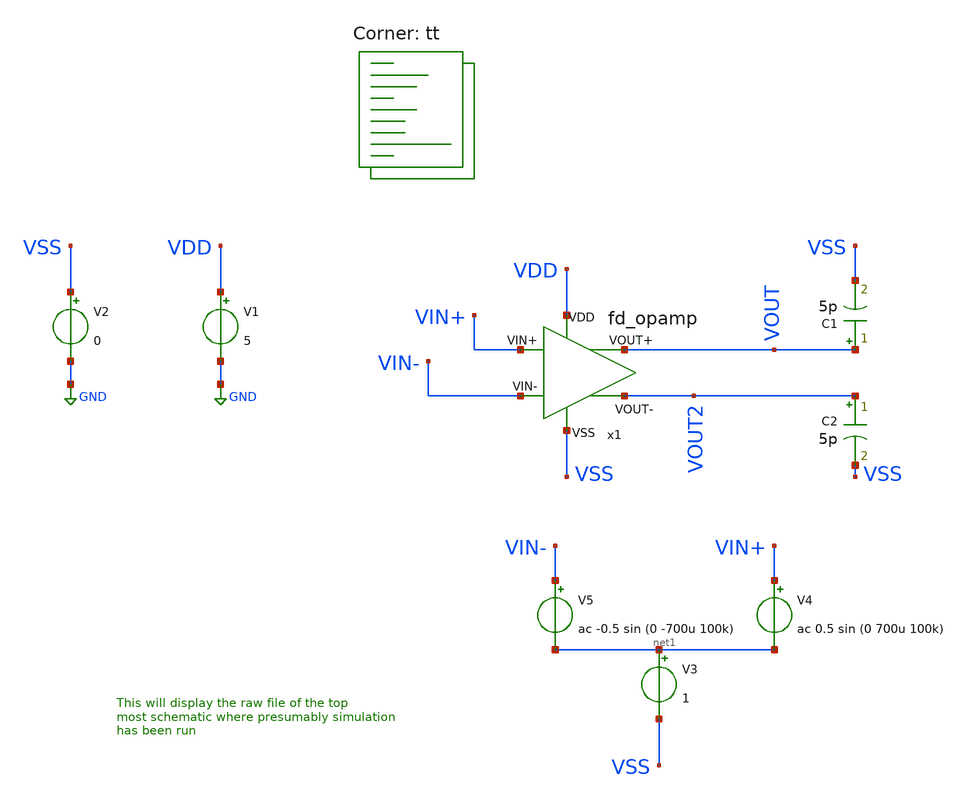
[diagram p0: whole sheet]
** sch_path: my_ip/sky130A/fully_differential_telescopic_cascode_5V_V1/tb/tb.sch
**.subckt tb
V1 VDD GND 5
V2 VSS GND 0
V3 net1 VSS 1
V4 VIN+ net1 ac 0.5 sin (0 700u 100k)
V5 VIN- net1 ac -0.5 sin (0 -700u 100k)
x1 VDD VSS VIN+ VOUT VIN- VOUT2 fd_opamp
C1 VOUT VSS 5p m=1
C2 VOUT2 VSS 5p m=1
**** begin user architecture code
.lib $::SKYWATER_MODELS/sky130.lib.spice tt
**** end user architecture code
**.ends
.GLOBAL GND
**** begin user architecture code


* ngspice commands
.options savecurrents
.TEMP 27
.control
save all
save @m.x1.xm1.msky130_fd_pr__pfet_g5v0d10v5[gm]
save @m.x1.xm1.msky130_fd_pr__pfet_g5v0d10v5[vth]
save @m.x1.xm1.msky130_fd_pr__pfet_g5v0d10v5[vds]
save @m.x1.xm1.msky130_fd_pr__pfet_g5v0d10v5[vgs]

save @m.x1.xm2.msky130_fd_pr__pfet_g5v0d10v5[gm]
save @m.x1.xm2.msky130_fd_pr__pfet_g5v0d10v5[vth]
save @m.x1.xm2.msky130_fd_pr__pfet_g5v0d10v5[vds]
save @m.x1.xm2.msky130_fd_pr__pfet_g5v0d10v5[vgs]

save @m.x1.xm3.msky130_fd_pr__pfet_g5v0d10v5[gm]
save @m.x1.xm3.msky130_fd_pr__pfet_g5v0d10v5[vth]
save @m.x1.xm3.msky130_fd_pr__pfet_g5v0d10v5[vds]
save @m.x1.xm3.msky130_fd_pr__pfet_g5v0d10v5[vgs]

save @m.x1.xm4.msky130_fd_pr__pfet_g5v0d10v5[gm]
save @m.x1.xm4.msky130_fd_pr__pfet_g5v0d10v5[vth]
save @m.x1.xm4.msky130_fd_pr__pfet_g5v0d10v5[vds]
save @m.x1.xm4.msky130_fd_pr__pfet_g5v0d10v5[vgs]

save @m.x1.xm5.msky130_fd_pr__nfet_g5v0d10v5[gm]
save @m.x1.xm5.msky130_fd_pr__nfet_g5v0d10v5[vth]
save @m.x1.xm5.msky130_fd_pr__nfet_g5v0d10v5[vds]
save @m.x1.xm5.msky130_fd_pr__nfet_g5v0d10v5[vgs]

save @m.x1.xm6.msky130_fd_pr__nfet_g5v0d10v5[gm]
save @m.x1.xm6.msky130_fd_pr__nfet_g5v0d10v5[vth]
save @m.x1.xm6.msky130_fd_pr__nfet_g5v0d10v5[vds]
save @m.x1.xm6.msky130_fd_pr__nfet_g5v0d10v5[vgs]

save @m.x1.xm7.msky130_fd_pr__nfet_g5v0d10v5[gm]
save @m.x1.xm7.msky130_fd_pr__nfet_g5v0d10v5[vth]
save @m.x1.xm7.msky130_fd_pr__nfet_g5v0d10v5[vds]
save @m.x1.xm7.msky130_fd_pr__nfet_g5v0d10v5[vgs]

save @m.x1.xm8.msky130_fd_pr__nfet_g5v0d10v5[gm]
save @m.x1.xm8.msky130_fd_pr__nfet_g5v0d10v5[vth]
save @m.x1.xm8.msky130_fd_pr__nfet_g5v0d10v5[vds]
save @m.x1.xm8.msky130_fd_pr__nfet_g5v0d10v5[vgs]

save @m.x1.xm9.msky130_fd_pr__pfet_g5v0d10v5[gm]
save @m.x1.xm9.msky130_fd_pr__pfet_g5v0d10v5[vth]
save @m.x1.xm9.msky130_fd_pr__pfet_g5v0d10v5[vds]
save @m.x1.xm9.msky130_fd_pr__pfet_g5v0d10v5[vgs]

save @m.x1.xm10.msky130_fd_pr__pfet_g5v0d10v5[gm]
save @m.x1.xm10.msky130_fd_pr__pfet_g5v0d10v5[vth]
save @m.x1.xm10.msky130_fd_pr__pfet_g5v0d10v5[vds]
save @m.x1.xm10.msky130_fd_pr__pfet_g5v0d10v5[vgs]

save @m.x1.xm11.msky130_fd_pr__pfet_g5v0d10v5[gm]
save @m.x1.xm11.msky130_fd_pr__pfet_g5v0d10v5[vth]
save @m.x1.xm11.msky130_fd_pr__pfet_g5v0d10v5[vds]
save @m.x1.xm11.msky130_fd_pr__pfet_g5v0d10v5[vgs]

save @m.x1.xm12.msky130_fd_pr__pfet_g5v0d10v5[gm]
save @m.x1.xm12.msky130_fd_pr__pfet_g5v0d10v5[vth]
save @m.x1.xm12.msky130_fd_pr__pfet_g5v0d10v5[vds]
save @m.x1.xm12.msky130_fd_pr__pfet_g5v0d10v5[vgs]

save @m.x1.xm13.msky130_fd_pr__nfet_g5v0d10v5[gm]
save @m.x1.xm13.msky130_fd_pr__nfet_g5v0d10v5[vth]
save @m.x1.xm13.msky130_fd_pr__nfet_g5v0d10v5[vds]
save @m.x1.xm13.msky130_fd_pr__nfet_g5v0d10v5[vgs]

save @m.x1.xm14.msky130_fd_pr__nfet_g5v0d10v5[gm]
save @m.x1.xm14.msky130_fd_pr__nfet_g5v0d10v5[vth]
save @m.x1.xm14.msky130_fd_pr__nfet_g5v0d10v5[vds]
save @m.x1.xm14.msky130_fd_pr__nfet_g5v0d10v5[vgs]

save @m.x1.xm15.msky130_fd_pr__nfet_g5v0d10v5[gm]
save @m.x1.xm15.msky130_fd_pr__nfet_g5v0d10v5[vth]
save @m.x1.xm15.msky130_fd_pr__nfet_g5v0d10v5[vds]
save @m.x1.xm15.msky130_fd_pr__nfet_g5v0d10v5[vgs]

save @m.x1.xm16.msky130_fd_pr__nfet_g5v0d10v5[gm]
save @m.x1.xm16.msky130_fd_pr__nfet_g5v0d10v5[vth]
save @m.x1.xm16.msky130_fd_pr__nfet_g5v0d10v5[vds]
save @m.x1.xm16.msky130_fd_pr__nfet_g5v0d10v5[vgs]


save @m.x1.xm17.msky130_fd_pr__pfet_g5v0d10v5[gm]
save @m.x1.xm17.msky130_fd_pr__pfet_g5v0d10v5[vth]
save @m.x1.xm17.msky130_fd_pr__pfet_g5v0d10v5[vds]
save @m.x1.xm17.msky130_fd_pr__pfet_g5v0d10v5[vgs]

save @m.x1.xm18.msky130_fd_pr__pfet_g5v0d10v5[gm]
save @m.x1.xm18.msky130_fd_pr__pfet_g5v0d10v5[vth]
save @m.x1.xm18.msky130_fd_pr__pfet_g5v0d10v5[vds]
save @m.x1.xm18.msky130_fd_pr__pfet_g5v0d10v5[vgs]

save @m.x1.xm19.msky130_fd_pr__pfet_g5v0d10v5[gm]
save @m.x1.xm19.msky130_fd_pr__pfet_g5v0d10v5[vth]
save @m.x1.xm19.msky130_fd_pr__pfet_g5v0d10v5[vds]
save @m.x1.xm19.msky130_fd_pr__pfet_g5v0d10v5[vgs]

save @m.x1.xm20.msky130_fd_pr__pfet_g5v0d10v5[gm]
save @m.x1.xm20.msky130_fd_pr__pfet_g5v0d10v5[vth]
save @m.x1.xm20.msky130_fd_pr__pfet_g5v0d10v5[vds]
save @m.x1.xm20.msky130_fd_pr__pfet_g5v0d10v5[vgs]

save @m.x1.xm21.msky130_fd_pr__pfet_g5v0d10v5[gm]
save @m.x1.xm21.msky130_fd_pr__pfet_g5v0d10v5[vth]
save @m.x1.xm21.msky130_fd_pr__pfet_g5v0d10v5[vds]
save @m.x1.xm21.msky130_fd_pr__pfet_g5v0d10v5[vgs]

save @m.x1.xm22.msky130_fd_pr__pfet_g5v0d10v5[gm]
save @m.x1.xm22.msky130_fd_pr__pfet_g5v0d10v5[vth]
save @m.x1.xm22.msky130_fd_pr__pfet_g5v0d10v5[vds]
save @m.x1.xm22.msky130_fd_pr__pfet_g5v0d10v5[vgs]

save @m.x1.xm23.msky130_fd_pr__nfet_g5v0d10v5[gm]
save @m.x1.xm23.msky130_fd_pr__nfet_g5v0d10v5[vth]
save @m.x1.xm23.msky130_fd_pr__nfet_g5v0d10v5[vds]
save @m.x1.xm23.msky130_fd_pr__nfet_g5v0d10v5[vgs]

save @m.x1.xm24.msky130_fd_pr__nfet_g5v0d10v5[gm]
save @m.x1.xm24.msky130_fd_pr__nfet_g5v0d10v5[vth]
save @m.x1.xm24.msky130_fd_pr__nfet_g5v0d10v5[vds]
save @m.x1.xm24.msky130_fd_pr__nfet_g5v0d10v5[vgs]

save @m.x1.xm25.msky130_fd_pr__nfet_g5v0d10v5[gm]
save @m.x1.xm25.msky130_fd_pr__nfet_g5v0d10v5[vth]
save @m.x1.xm25.msky130_fd_pr__nfet_g5v0d10v5[vds]
save @m.x1.xm25.msky130_fd_pr__nfet_g5v0d10v5[vgs]

save @m.x1.xm26.msky130_fd_pr__pfet_g5v0d10v5[gm]
save @m.x1.xm26.msky130_fd_pr__pfet_g5v0d10v5[vth]
save @m.x1.xm26.msky130_fd_pr__pfet_g5v0d10v5[vds]
save @m.x1.xm26.msky130_fd_pr__pfet_g5v0d10v5[vgs]

save @m.x1.xm27.msky130_fd_pr__pfet_g5v0d10v5[gm]
save @m.x1.xm27.msky130_fd_pr__pfet_g5v0d10v5[vth]
save @m.x1.xm27.msky130_fd_pr__pfet_g5v0d10v5[vds]
save @m.x1.xm27.msky130_fd_pr__pfet_g5v0d10v5[vgs]

save @m.x1.xm28.msky130_fd_pr__nfet_g5v0d10v5[gm]
save @m.x1.xm28.msky130_fd_pr__nfet_g5v0d10v5[vth]
save @m.x1.xm28.msky130_fd_pr__nfet_g5v0d10v5[vds]
save @m.x1.xm28.msky130_fd_pr__nfet_g5v0d10v5[vgs]

op
write tb.raw

ac dec 10 1 50G
plot db(v(VOUT)) (180*ph(v(VOUT))/pi)
set appendwrite
write tb.raw

tran 1ns 100u
plot v(VOUT) v(VOUT2)
set appendwrite
write tb.raw
.endc



**** end user architecture code
.end
